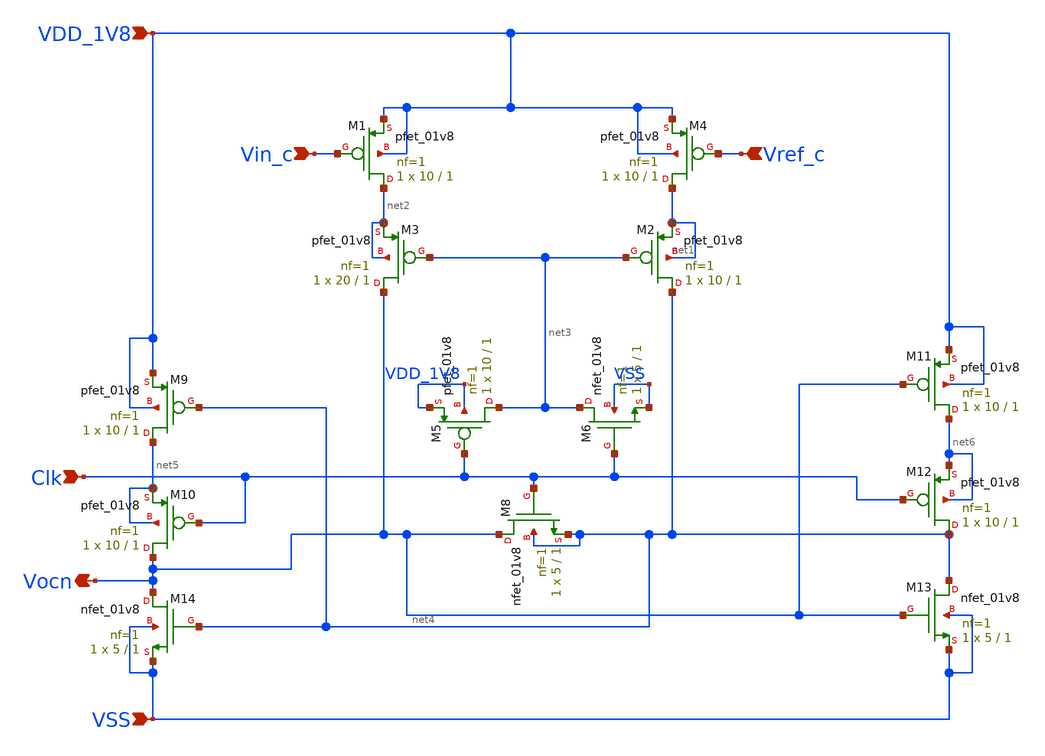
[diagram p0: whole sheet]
** sch_path: design/CNR_GR06_SKY130NM/comparator.sch
**.subckt comparator Vin_c Vref_c Clk VSS VDD_1V8 Vocn
*.ipin Vin_c
*.ipin Vref_c
*.ipin Clk
*.ipin VSS
*.ipin VDD_1V8
*.opin Vocn
XM8 Vocn Clk net4 net4 sky130_fd_pr__nfet_01v8 L=1 W=5 nf=1 ad='int((nf+1)/2) * W/nf * 0.29' as='int((nf+2)/2) * W/nf * 0.29'
+ pd='2*int((nf+1)/2) * (W/nf + 0.29)' ps='2*int((nf+2)/2) * (W/nf + 0.29)' nrd='0.29 / W' nrs='0.29 / W'
+ sa=0 sb=0 sd=0 mult=1 m=1
XM6 net3 Clk VSS VSS sky130_fd_pr__nfet_01v8 L=1 W=5 nf=1 ad='int((nf+1)/2) * W/nf * 0.29' as='int((nf+2)/2) * W/nf * 0.29'
+ pd='2*int((nf+1)/2) * (W/nf + 0.29)' ps='2*int((nf+2)/2) * (W/nf + 0.29)' nrd='0.29 / W' nrs='0.29 / W'
+ sa=0 sb=0 sd=0 mult=1 m=1
XM1 net2 Vin_c VDD_1V8 VDD_1V8 sky130_fd_pr__pfet_01v8 L=1 W=10 nf=1 ad='int((nf+1)/2) * W/nf * 0.29'
+ as='int((nf+2)/2) * W/nf * 0.29' pd='2*int((nf+1)/2) * (W/nf + 0.29)' ps='2*int((nf+2)/2) * (W/nf + 0.29)'
+ nrd='0.29 / W' nrs='0.29 / W' sa=0 sb=0 sd=0 mult=1 m=1
XM2 net4 net3 net1 net1 sky130_fd_pr__pfet_01v8 L=1 W=10 nf=1 ad='int((nf+1)/2) * W/nf * 0.29' as='int((nf+2)/2) * W/nf * 0.29'
+ pd='2*int((nf+1)/2) * (W/nf + 0.29)' ps='2*int((nf+2)/2) * (W/nf + 0.29)' nrd='0.29 / W' nrs='0.29 / W'
+ sa=0 sb=0 sd=0 mult=1 m=1
XM3 Vocn net3 net2 net2 sky130_fd_pr__pfet_01v8 L=1 W=20 nf=1 ad='int((nf+1)/2) * W/nf * 0.29' as='int((nf+2)/2) * W/nf * 0.29'
+ pd='2*int((nf+1)/2) * (W/nf + 0.29)' ps='2*int((nf+2)/2) * (W/nf + 0.29)' nrd='0.29 / W' nrs='0.29 / W'
+ sa=0 sb=0 sd=0 mult=1 m=1
XM4 net1 Vref_c VDD_1V8 VDD_1V8 sky130_fd_pr__pfet_01v8 L=1 W=10 nf=1 ad='int((nf+1)/2) * W/nf * 0.29'
+ as='int((nf+2)/2) * W/nf * 0.29' pd='2*int((nf+1)/2) * (W/nf + 0.29)' ps='2*int((nf+2)/2) * (W/nf + 0.29)'
+ nrd='0.29 / W' nrs='0.29 / W' sa=0 sb=0 sd=0 mult=1 m=1
XM5 net3 Clk VDD_1V8 VDD_1V8 sky130_fd_pr__pfet_01v8 L=1 W=10 nf=1 ad='int((nf+1)/2) * W/nf * 0.29' as='int((nf+2)/2) * W/nf * 0.29'
+ pd='2*int((nf+1)/2) * (W/nf + 0.29)' ps='2*int((nf+2)/2) * (W/nf + 0.29)' nrd='0.29 / W' nrs='0.29 / W'
+ sa=0 sb=0 sd=0 mult=1 m=1
XM9 net5 net4 VDD_1V8 VDD_1V8 sky130_fd_pr__pfet_01v8 L=1 W=10 nf=1 ad='int((nf+1)/2) * W/nf * 0.29'
+ as='int((nf+2)/2) * W/nf * 0.29' pd='2*int((nf+1)/2) * (W/nf + 0.29)' ps='2*int((nf+2)/2) * (W/nf + 0.29)'
+ nrd='0.29 / W' nrs='0.29 / W' sa=0 sb=0 sd=0 mult=1 m=1
XM10 Vocn Clk net5 net5 sky130_fd_pr__pfet_01v8 L=1 W=10 nf=1 ad='int((nf+1)/2) * W/nf * 0.29' as='int((nf+2)/2) * W/nf * 0.29'
+ pd='2*int((nf+1)/2) * (W/nf + 0.29)' ps='2*int((nf+2)/2) * (W/nf + 0.29)' nrd='0.29 / W' nrs='0.29 / W'
+ sa=0 sb=0 sd=0 mult=1 m=1
XM11 net6 Vocn VDD_1V8 VDD_1V8 sky130_fd_pr__pfet_01v8 L=1 W=10 nf=1 ad='int((nf+1)/2) * W/nf * 0.29'
+ as='int((nf+2)/2) * W/nf * 0.29' pd='2*int((nf+1)/2) * (W/nf + 0.29)' ps='2*int((nf+2)/2) * (W/nf + 0.29)'
+ nrd='0.29 / W' nrs='0.29 / W' sa=0 sb=0 sd=0 mult=1 m=1
XM12 net4 Clk net6 net6 sky130_fd_pr__pfet_01v8 L=1 W=10 nf=1 ad='int((nf+1)/2) * W/nf * 0.29' as='int((nf+2)/2) * W/nf * 0.29'
+ pd='2*int((nf+1)/2) * (W/nf + 0.29)' ps='2*int((nf+2)/2) * (W/nf + 0.29)' nrd='0.29 / W' nrs='0.29 / W'
+ sa=0 sb=0 sd=0 mult=1 m=1
XM13 net4 Vocn VSS VSS sky130_fd_pr__nfet_01v8 L=1 W=5 nf=1 ad='int((nf+1)/2) * W/nf * 0.29' as='int((nf+2)/2) * W/nf * 0.29'
+ pd='2*int((nf+1)/2) * (W/nf + 0.29)' ps='2*int((nf+2)/2) * (W/nf + 0.29)' nrd='0.29 / W' nrs='0.29 / W'
+ sa=0 sb=0 sd=0 mult=1 m=1
XM14 Vocn net4 VSS VSS sky130_fd_pr__nfet_01v8 L=1 W=5 nf=1 ad='int((nf+1)/2) * W/nf * 0.29' as='int((nf+2)/2) * W/nf * 0.29'
+ pd='2*int((nf+1)/2) * (W/nf + 0.29)' ps='2*int((nf+2)/2) * (W/nf + 0.29)' nrd='0.29 / W' nrs='0.29 / W'
+ sa=0 sb=0 sd=0 mult=1 m=1
**.ends
.end
